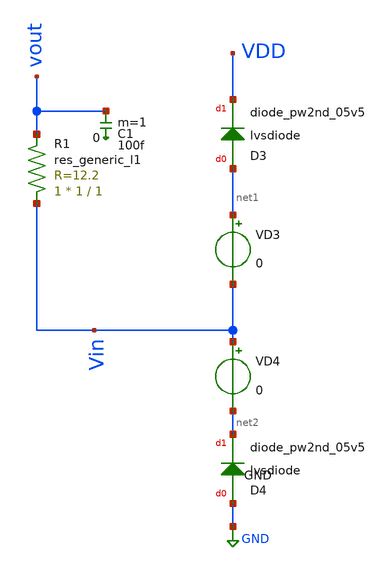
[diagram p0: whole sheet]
** sch_path: sky130_cells/ESD_Diode/ESD_Flatten.sch
**.subckt ESD_Flatten
D3 net1 VDD sky130_fd_pr__diode_pw2nd_05v5 area=1e12
D4 GND net2 sky130_fd_pr__diode_pw2nd_05v5 area=1e12
R1 Vin vout sky130_fd_pr__res_generic_l1 W=1 L=1 m=1
VD3 net1 Vin 0
C1 vout 0 100f m=1
VD4 Vin net2 0
**.ends
.GLOBAL GND
.end
